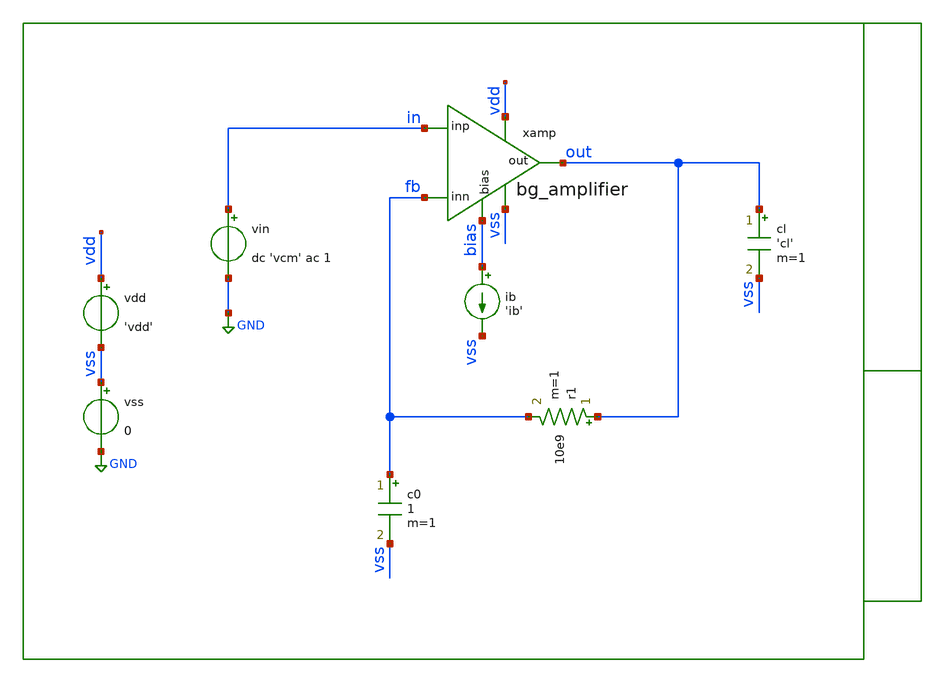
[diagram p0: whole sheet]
** sch_path: xschem/tb/bandgap_cm/bg_amplifier/no_bg_amplifier.sch
**.subckt no_bg_amplifier
vin in GND dc 'vcm' ac 1
c0 fb vss 1 m=1
r1 out fb 10e9 m=1
ib bias vss 'ib'
vdd vdd vss 'vdd'
vss vss GND 0
cl out vss 'cl' m=1
xamp vdd out in fb vss bias bg_amplifier
**** begin user architecture code

* Control

.param vdd=3.3
.param vcm='vdd/2'
.param ib=1u
.param cl=1p

.control
save all
noise v(out,vss) vin dec 10 0.1 1e6 1
print inoise_total
print onoise_total
setplot noise1
gnuplot p1 inoise_spectrum
gnuplot p2 onoise_spectrum
set wr_singlescale
set wr_vecnames
wrdata data.csv onoise_spectrum inoise_spectrum
.endc


 * Model Corners

.include $::CORNERS/ngspice/tt.spice
*.include $::CORNERS/ngspice/ff.spice
*.include $::CORNERS/ngspice/ss.spice
*.include $::CORNERS/ngspice/sf.spice
*.include $::CORNERS/ngspice/fs.spice

 * extract

* pex
*.include $::DESIGN_PATH/sch/bandgap_cm/bg_amplifier/bg_amplifier.pex.spice

**** end user architecture code
**.ends

* expanding   symbol:  sch/bandgap_cm/bg_amplifier/bg_amplifier.sym # of pins=6
** sym_path: xschem/sch/bandgap_cm/bg_amplifier/bg_amplifier.sym
** sch_path: xschem/sch/bandgap_cm/bg_amplifier/bg_amplifier.sch
.subckt bg_amplifier vdd out inp inn vss bias
*.ipin inn
*.ipin inp
*.opin out
*.iopin bias
*.iopin vdd
*.iopin vss
XMB5 vbn1 vbn1 vss vss nfet_06v0 L=2u W=16u nf=2 ad='int((nf+1)/2) * W/nf * 0.18u' as='int((nf+2)/2) * W/nf * 0.18u'
+ pd='2*int((nf+1)/2) * (W/nf + 0.18u)' ps='2*int((nf+2)/2) * (W/nf + 0.18u)' nrd='0.18u / W' nrs='0.18u / W'
+ sa=0 sb=0 sd=0 m=4 par=4
XMC1 von vbn1 vss vss nfet_06v0 L=2u W=16u nf=2 ad='int((nf+1)/2) * W/nf * 0.18u' as='int((nf+2)/2) * W/nf * 0.18u'
+ pd='2*int((nf+1)/2) * (W/nf + 0.18u)' ps='2*int((nf+2)/2) * (W/nf + 0.18u)' nrd='0.18u / W' nrs='0.18u / W'
+ sa=0 sb=0 sd=0 m=10 par=10
XMC2 vop vbn1 vss vss nfet_06v0 L=2u W=16u nf=2 ad='int((nf+1)/2) * W/nf * 0.18u' as='int((nf+2)/2) * W/nf * 0.18u'
+ pd='2*int((nf+1)/2) * (W/nf + 0.18u)' ps='2*int((nf+2)/2) * (W/nf + 0.18u)' nrd='0.18u / W' nrs='0.18u / W'
+ sa=0 sb=0 sd=0 m=10 par=10
XMC3 mirr vbn2 von vss nfet_06v0 L=2u W=16u nf=2 ad='int((nf+1)/2) * W/nf * 0.18u' as='int((nf+2)/2) * W/nf * 0.18u'
+ pd='2*int((nf+1)/2) * (W/nf + 0.18u)' ps='2*int((nf+2)/2) * (W/nf + 0.18u)' nrd='0.18u / W' nrs='0.18u / W'
+ sa=0 sb=0 sd=0 m=4 par=4
XMC4 out vbn2 vop vss nfet_06v0 L=2u W=16u nf=2 ad='int((nf+1)/2) * W/nf * 0.18u' as='int((nf+2)/2) * W/nf * 0.18u'
+ pd='2*int((nf+1)/2) * (W/nf + 0.18u)' ps='2*int((nf+2)/2) * (W/nf + 0.18u)' nrd='0.18u / W' nrs='0.18u / W'
+ sa=0 sb=0 sd=0 m=4 par=4
XMB3 bias bias vbp1 vdd pfet_06v0 L=2u W=16u nf=2 ad='int((nf+1)/2) * W/nf * 0.18u' as='int((nf+2)/2) * W/nf * 0.18u'
+ pd='2*int((nf+1)/2) * (W/nf + 0.18u)' ps='2*int((nf+2)/2) * (W/nf + 0.18u)' nrd='0.18u / W' nrs='0.18u / W'
+ sa=0 sb=0 sd=0 m=2 par=2
XMB1 vbp1 vbp1 vdd vdd pfet_06v0 L=2u W=16u nf=2 ad='int((nf+1)/2) * W/nf * 0.18u' as='int((nf+2)/2) * W/nf * 0.18u'
+ pd='2*int((nf+1)/2) * (W/nf + 0.18u)' ps='2*int((nf+2)/2) * (W/nf + 0.18u)' nrd='0.18u / W' nrs='0.18u / W'
+ sa=0 sb=0 sd=0 m=4 par=4
XMB2 vbn2 vbp1 vdd vdd pfet_06v0 L=2u W=16u nf=2 ad='int((nf+1)/2) * W/nf * 0.18u' as='int((nf+2)/2) * W/nf * 0.18u'
+ pd='2*int((nf+1)/2) * (W/nf + 0.18u)' ps='2*int((nf+2)/2) * (W/nf + 0.18u)' nrd='0.18u / W' nrs='0.18u / W'
+ sa=0 sb=0 sd=0 m=4 par=4
XMT1 vcm vbp1 vdd vdd pfet_06v0 L=2u W=16u nf=2 ad='int((nf+1)/2) * W/nf * 0.18u' as='int((nf+2)/2) * W/nf * 0.18u'
+ pd='2*int((nf+1)/2) * (W/nf + 0.18u)' ps='2*int((nf+2)/2) * (W/nf + 0.18u)' nrd='0.18u / W' nrs='0.18u / W'
+ sa=0 sb=0 sd=0 m=8 par=8
XMD1 von inp vcm vdd pfet_06v0 L=4u W=16u nf=2 ad='int((nf+1)/2) * W/nf * 0.18u' as='int((nf+2)/2) * W/nf * 0.18u'
+ pd='2*int((nf+1)/2) * (W/nf + 0.18u)' ps='2*int((nf+2)/2) * (W/nf + 0.18u)' nrd='0.18u / W' nrs='0.18u / W'
+ sa=0 sb=0 sd=0 m=4 par=4
XMD2 vop inn vcm vdd pfet_06v0 L=4u W=16u nf=2 ad='int((nf+1)/2) * W/nf * 0.18u' as='int((nf+2)/2) * W/nf * 0.18u'
+ pd='2*int((nf+1)/2) * (W/nf + 0.18u)' ps='2*int((nf+2)/2) * (W/nf + 0.18u)' nrd='0.18u / W' nrs='0.18u / W'
+ sa=0 sb=0 sd=0 m=4 par=4
XMC7 vda mirr vdd vdd pfet_06v0 L=2u W=16u nf=2 ad='int((nf+1)/2) * W/nf * 0.18u' as='int((nf+2)/2) * W/nf * 0.18u'
+ pd='2*int((nf+1)/2) * (W/nf + 0.18u)' ps='2*int((nf+2)/2) * (W/nf + 0.18u)' nrd='0.18u / W' nrs='0.18u / W'
+ sa=0 sb=0 sd=0 m=2 par=2
XMC8 vdb mirr vdd vdd pfet_06v0 L=2u W=16u nf=2 ad='int((nf+1)/2) * W/nf * 0.18u' as='int((nf+2)/2) * W/nf * 0.18u'
+ pd='2*int((nf+1)/2) * (W/nf + 0.18u)' ps='2*int((nf+2)/2) * (W/nf + 0.18u)' nrd='0.18u / W' nrs='0.18u / W'
+ sa=0 sb=0 sd=0 m=2 par=2
XMC5 mirr bias vda vdd pfet_06v0 L=2u W=16u nf=2 ad='int((nf+1)/2) * W/nf * 0.18u' as='int((nf+2)/2) * W/nf * 0.18u'
+ pd='2*int((nf+1)/2) * (W/nf + 0.18u)' ps='2*int((nf+2)/2) * (W/nf + 0.18u)' nrd='0.18u / W' nrs='0.18u / W'
+ sa=0 sb=0 sd=0 m=4 par=4
XMC6 out bias vdb vdd pfet_06v0 L=2u W=16u nf=2 ad='int((nf+1)/2) * W/nf * 0.18u' as='int((nf+2)/2) * W/nf * 0.18u'
+ pd='2*int((nf+1)/2) * (W/nf + 0.18u)' ps='2*int((nf+2)/2) * (W/nf + 0.18u)' nrd='0.18u / W' nrs='0.18u / W'
+ sa=0 sb=0 sd=0 m=4 par=4
XMB4 vbn2 vbn2 vbn1 vss nfet_06v0 L=2u W=16u nf=2 ad='int((nf+1)/2) * W/nf * 0.18u' as='int((nf+2)/2) * W/nf * 0.18u'
+ pd='2*int((nf+1)/2) * (W/nf + 0.18u)' ps='2*int((nf+2)/2) * (W/nf + 0.18u)' nrd='0.18u / W' nrs='0.18u / W'
+ sa=0 sb=0 sd=0 m=4 par=4
XMDUM1 vdd vdd vdd vdd pfet_06v0 L=2u W=16u nf=2 ad='int((nf+1)/2) * W/nf * 0.18u' as='int((nf+2)/2) * W/nf * 0.18u'
+ pd='2*int((nf+1)/2) * (W/nf + 0.18u)' ps='2*int((nf+2)/2) * (W/nf + 0.18u)' nrd='0.18u / W' nrs='0.18u / W'
+ sa=0 sb=0 sd=0 m=4 par=4
XMDUM2 vdd vdd vdd vdd pfet_06v0 L=2u W=16u nf=2 ad='int((nf+1)/2) * W/nf * 0.18u' as='int((nf+2)/2) * W/nf * 0.18u'
+ pd='2*int((nf+1)/2) * (W/nf + 0.18u)' ps='2*int((nf+2)/2) * (W/nf + 0.18u)' nrd='0.18u / W' nrs='0.18u / W'
+ sa=0 sb=0 sd=0 m=4 par=4
XMDUM3 vdd vdd vdd vdd pfet_06v0 L=2u W=16u nf=2 ad='int((nf+1)/2) * W/nf * 0.18u' as='int((nf+2)/2) * W/nf * 0.18u'
+ pd='2*int((nf+1)/2) * (W/nf + 0.18u)' ps='2*int((nf+2)/2) * (W/nf + 0.18u)' nrd='0.18u / W' nrs='0.18u / W'
+ sa=0 sb=0 sd=0 m=2 par=2
XMDUM4 vss vss vss vss nfet_06v0 L=2u W=16u nf=2 ad='int((nf+1)/2) * W/nf * 0.18u' as='int((nf+2)/2) * W/nf * 0.18u'
+ pd='2*int((nf+1)/2) * (W/nf + 0.18u)' ps='2*int((nf+2)/2) * (W/nf + 0.18u)' nrd='0.18u / W' nrs='0.18u / W'
+ sa=0 sb=0 sd=0 m=2 par=2
XMDUM5 vss vss vss vss nfet_06v0 L=2u W=16u nf=2 ad='int((nf+1)/2) * W/nf * 0.18u' as='int((nf+2)/2) * W/nf * 0.18u'
+ pd='2*int((nf+1)/2) * (W/nf + 0.18u)' ps='2*int((nf+2)/2) * (W/nf + 0.18u)' nrd='0.18u / W' nrs='0.18u / W'
+ sa=0 sb=0 sd=0 m=2 par=2
XMDUM6 vdd vdd vdd vdd pfet_06v0 L=4u W=16u nf=2 ad='int((nf+1)/2) * W/nf * 0.18u' as='int((nf+2)/2) * W/nf * 0.18u'
+ pd='2*int((nf+1)/2) * (W/nf + 0.18u)' ps='2*int((nf+2)/2) * (W/nf + 0.18u)' nrd='0.18u / W' nrs='0.18u / W'
+ sa=0 sb=0 sd=0 m=16 par=16
.ends

.GLOBAL GND
.end
